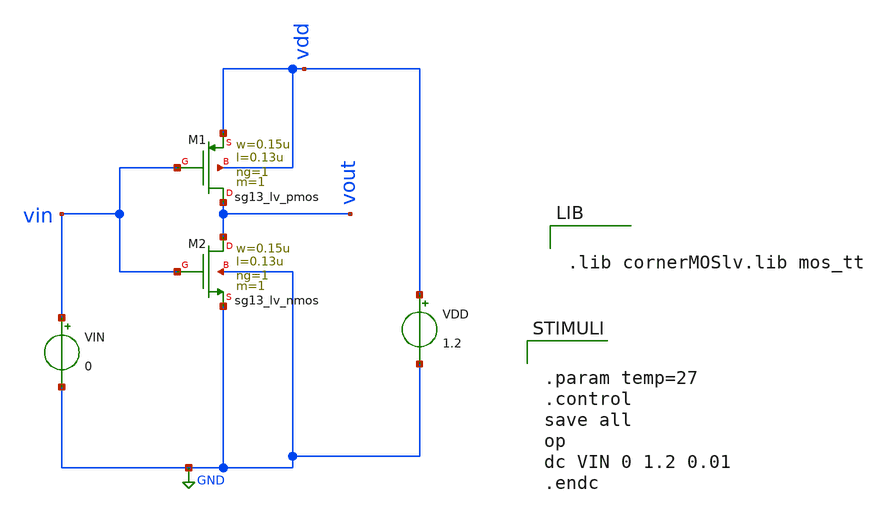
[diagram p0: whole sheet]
** sch_path: lab2-2.sch
**.subckt lab2-2
VIN vin GND 0
XM2 vout vin GND GND sg13_lv_nmos w=0.15u l=0.13u ng=1 m=1 mm_ok=1
VDD vdd GND 1.2
XM1 vout vin vdd vdd sg13_lv_pmos w=0.15u l=0.13u ng=1 m=1 mm_ok=1
**** begin user architecture code


.lib cornerMOSlv.lib mos_tt



.param temp=27
.control
save all
op
dc VIN 0 1.2 0.01
.endc


**** end user architecture code
**.ends
.GLOBAL GND
.end
